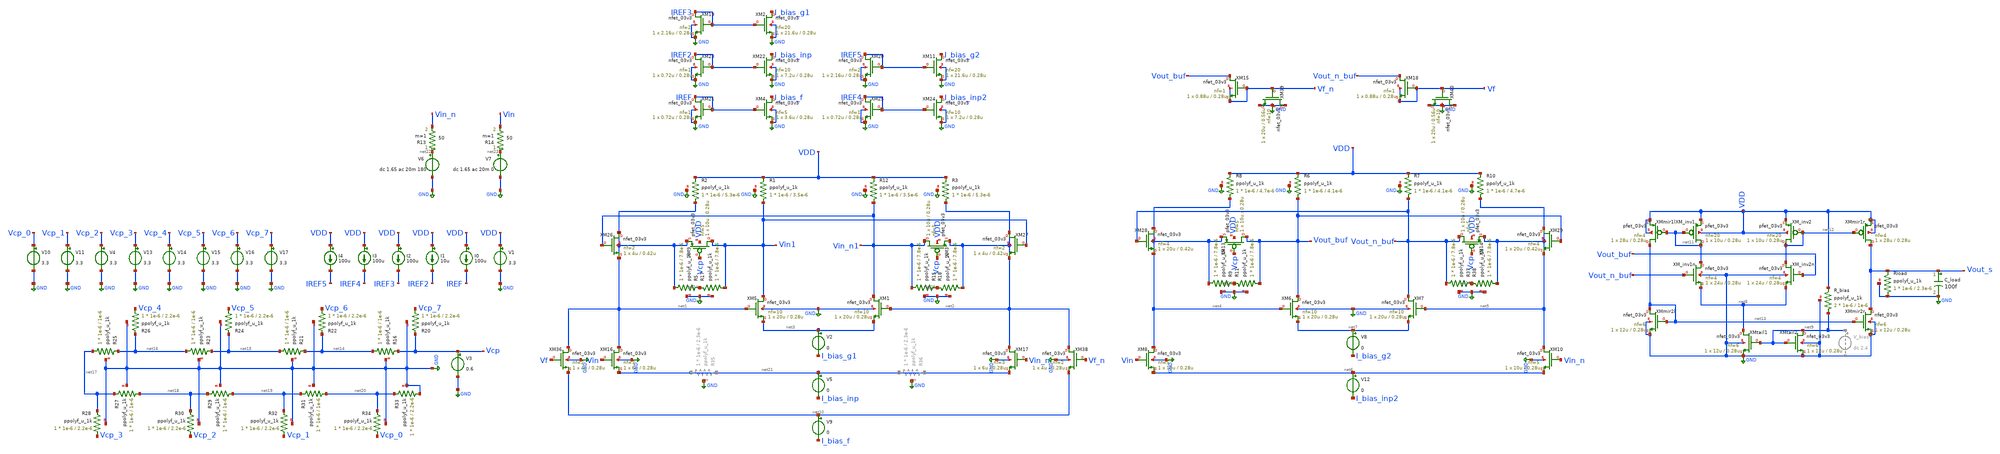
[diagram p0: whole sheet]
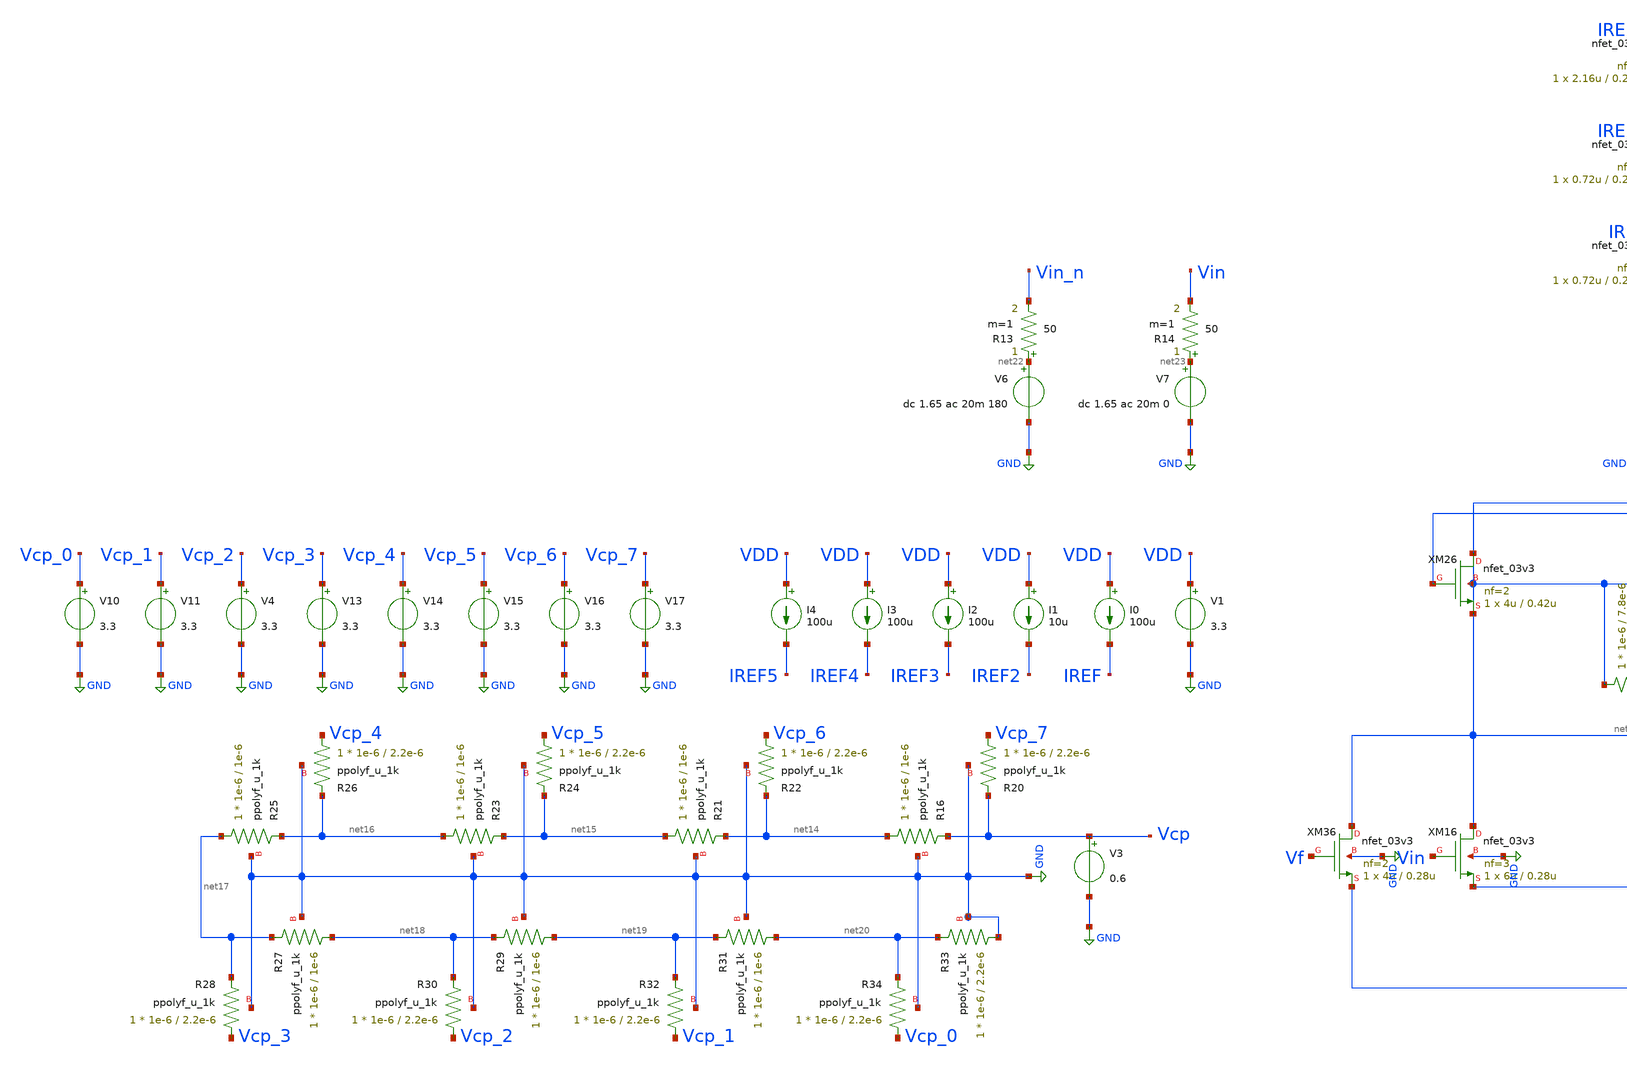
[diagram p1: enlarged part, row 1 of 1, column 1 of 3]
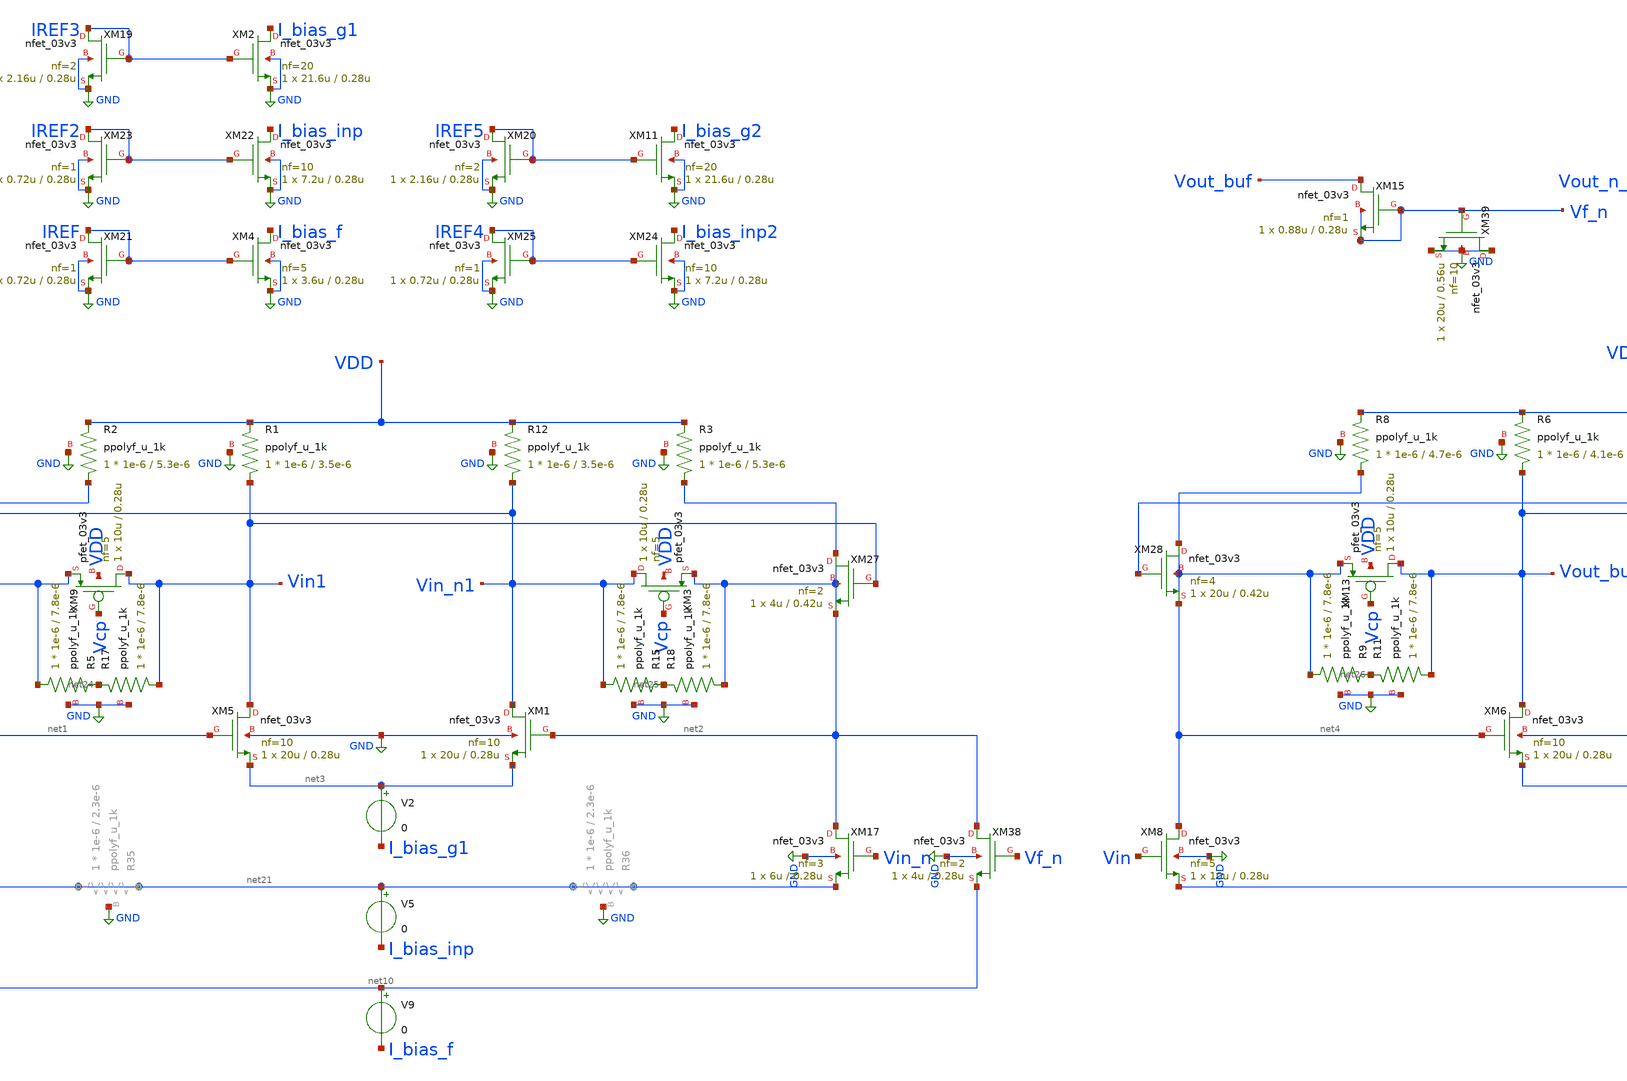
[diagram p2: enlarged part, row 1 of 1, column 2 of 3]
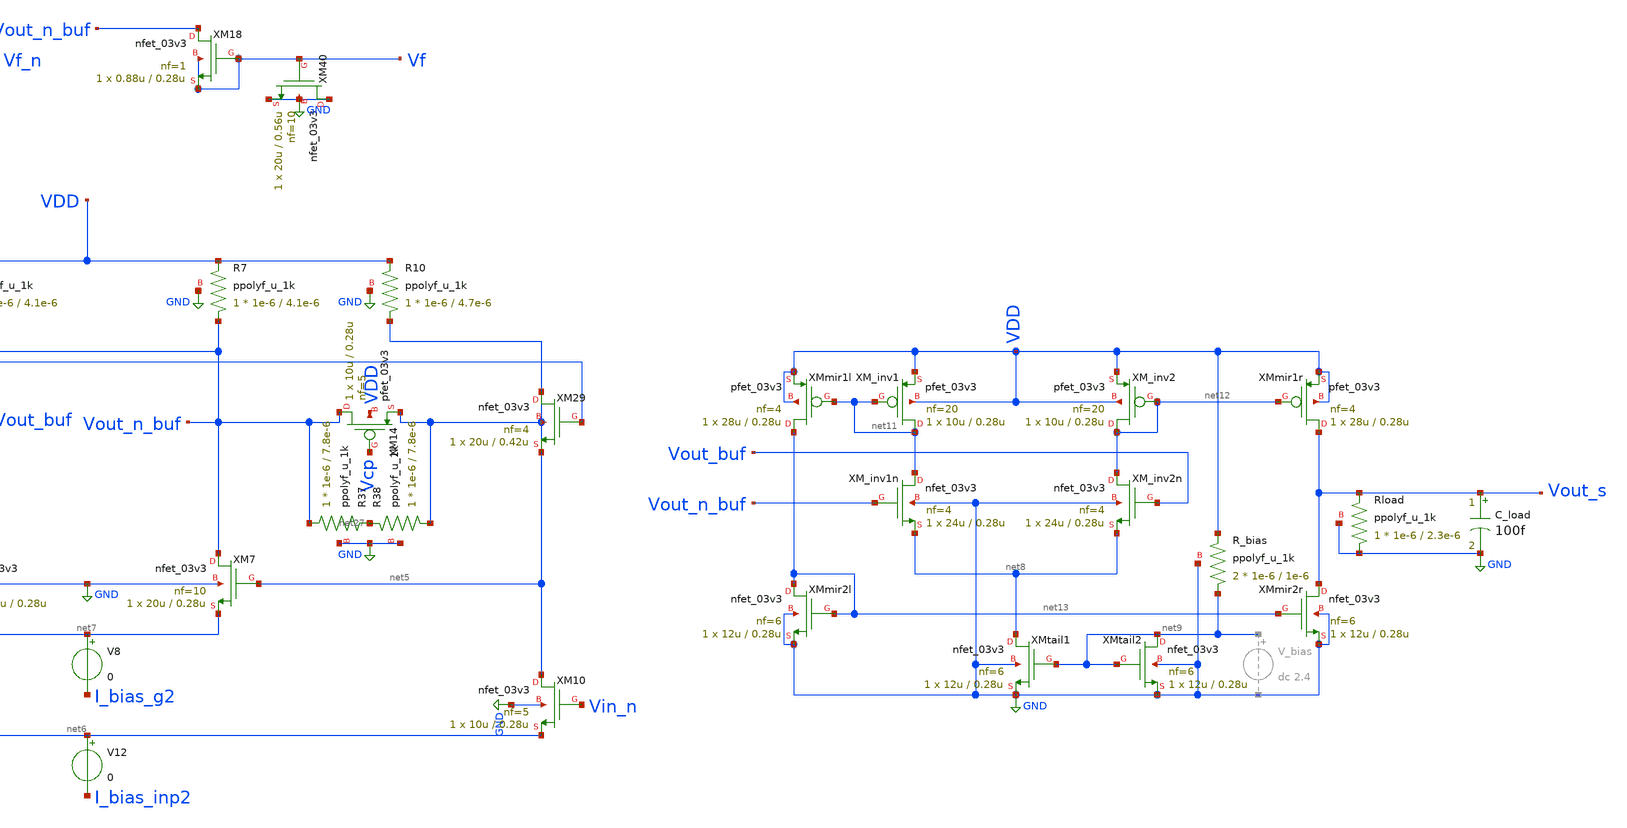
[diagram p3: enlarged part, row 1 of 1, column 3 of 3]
** sch_path: blocks/vga/vga.sch
**.subckt vga
V1 VDD GND 3.3
V6 net22 GND dc 1.65 ac 20m 180
XM5 Vin1 net1 net3 GND nfet_03v3 L=0.28u W=20u nf=10 ad='int((nf+1)/2) * W/nf * 0.18u' as='int((nf+2)/2) * W/nf * 0.18u'
+ pd='2*int((nf+1)/2) * (W/nf + 0.18u)' ps='2*int((nf+2)/2) * (W/nf + 0.18u)' nrd='0.18u / W' nrs='0.18u / W'
+ sa=0 sb=0 sd=0 m=1
XM1 Vin_n1 net2 net3 GND nfet_03v3 L=0.28u W=20u nf=10 ad='int((nf+1)/2) * W/nf * 0.18u' as='int((nf+2)/2) * W/nf * 0.18u'
+ pd='2*int((nf+1)/2) * (W/nf + 0.18u)' ps='2*int((nf+2)/2) * (W/nf + 0.18u)' nrd='0.18u / W' nrs='0.18u / W'
+ sa=0 sb=0 sd=0 m=1
XM16 net1 Vin net21 GND nfet_03v3 L=0.28u W=6u nf=3 ad='int((nf+1)/2) * W/nf * 0.18u' as='int((nf+2)/2) * W/nf * 0.18u'
+ pd='2*int((nf+1)/2) * (W/nf + 0.18u)' ps='2*int((nf+2)/2) * (W/nf + 0.18u)' nrd='0.18u / W' nrs='0.18u / W'
+ sa=0 sb=0 sd=0 m=1
XM17 net2 Vin_n net21 GND nfet_03v3 L=0.28u W=6u nf=3 ad='int((nf+1)/2) * W/nf * 0.18u' as='int((nf+2)/2) * W/nf * 0.18u'
+ pd='2*int((nf+1)/2) * (W/nf + 0.18u)' ps='2*int((nf+2)/2) * (W/nf + 0.18u)' nrd='0.18u / W' nrs='0.18u / W'
+ sa=0 sb=0 sd=0 m=1
XM9 Vin1 Vcp net1 VDD pfet_03v3 L=0.28u W=10u nf=5 ad='int((nf+1)/2) * W/nf * 0.18u' as='int((nf+2)/2) * W/nf * 0.18u'
+ pd='2*int((nf+1)/2) * (W/nf + 0.18u)' ps='2*int((nf+2)/2) * (W/nf + 0.18u)' nrd='0.18u / W' nrs='0.18u / W'
+ sa=0 sb=0 sd=0 m=1
XM6 Vout_buf net4 net7 GND nfet_03v3 L=0.28u W=20u nf=10 ad='int((nf+1)/2) * W/nf * 0.18u' as='int((nf+2)/2) * W/nf * 0.18u'
+ pd='2*int((nf+1)/2) * (W/nf + 0.18u)' ps='2*int((nf+2)/2) * (W/nf + 0.18u)' nrd='0.18u / W' nrs='0.18u / W'
+ sa=0 sb=0 sd=0 m=1
XM7 Vout_n_buf net5 net7 GND nfet_03v3 L=0.28u W=20u nf=10 ad='int((nf+1)/2) * W/nf * 0.18u' as='int((nf+2)/2) * W/nf * 0.18u'
+ pd='2*int((nf+1)/2) * (W/nf + 0.18u)' ps='2*int((nf+2)/2) * (W/nf + 0.18u)' nrd='0.18u / W' nrs='0.18u / W'
+ sa=0 sb=0 sd=0 m=1
XM8 net4 Vin net6 GND nfet_03v3 L=0.28u W=10u nf=5 ad='int((nf+1)/2) * W/nf * 0.18u' as='int((nf+2)/2) * W/nf * 0.18u'
+ pd='2*int((nf+1)/2) * (W/nf + 0.18u)' ps='2*int((nf+2)/2) * (W/nf + 0.18u)' nrd='0.18u / W' nrs='0.18u / W'
+ sa=0 sb=0 sd=0 m=1
XM10 net5 Vin_n net6 GND nfet_03v3 L=0.28u W=10u nf=5 ad='int((nf+1)/2) * W/nf * 0.18u' as='int((nf+2)/2) * W/nf * 0.18u'
+ pd='2*int((nf+1)/2) * (W/nf + 0.18u)' ps='2*int((nf+2)/2) * (W/nf + 0.18u)' nrd='0.18u / W' nrs='0.18u / W'
+ sa=0 sb=0 sd=0 m=1
V7 net23 GND dc 1.65 ac 20m 0
R14 net23 Vin 50 m=1
R13 net22 Vin_n 50 m=1
XM26 net1 Vin_n1 net1 net1 nfet_03v3 L=0.42u W=4u nf=2 ad='int((nf+1)/2) * W/nf * 0.18u' as='int((nf+2)/2) * W/nf * 0.18u'
+ pd='2*int((nf+1)/2) * (W/nf + 0.18u)' ps='2*int((nf+2)/2) * (W/nf + 0.18u)' nrd='0.18u / W' nrs='0.18u / W'
+ sa=0 sb=0 sd=0 m=1
XM27 net2 Vin1 net2 net2 nfet_03v3 L=0.42u W=4u nf=2 ad='int((nf+1)/2) * W/nf * 0.18u' as='int((nf+2)/2) * W/nf * 0.18u'
+ pd='2*int((nf+1)/2) * (W/nf + 0.18u)' ps='2*int((nf+2)/2) * (W/nf + 0.18u)' nrd='0.18u / W' nrs='0.18u / W'
+ sa=0 sb=0 sd=0 m=1
XM28 net4 Vout_n_buf net4 net4 nfet_03v3 L=0.42u W=20u nf=4 ad='int((nf+1)/2) * W/nf * 0.18u' as='int((nf+2)/2) * W/nf * 0.18u'
+ pd='2*int((nf+1)/2) * (W/nf + 0.18u)' ps='2*int((nf+2)/2) * (W/nf + 0.18u)' nrd='0.18u / W' nrs='0.18u / W'
+ sa=0 sb=0 sd=0 m=1
XM29 net5 Vout_buf net5 net5 nfet_03v3 L=0.42u W=20u nf=4 ad='int((nf+1)/2) * W/nf * 0.18u' as='int((nf+2)/2) * W/nf * 0.18u'
+ pd='2*int((nf+1)/2) * (W/nf + 0.18u)' ps='2*int((nf+2)/2) * (W/nf + 0.18u)' nrd='0.18u / W' nrs='0.18u / W'
+ sa=0 sb=0 sd=0 m=1
XM_inv1 net11 net11 VDD VDD pfet_03v3 L=0.28u W=10u nf=20 ad='int((nf+1)/2) * W/nf * 0.18u' as='int((nf+2)/2) * W/nf * 0.18u'
+ pd='2*int((nf+1)/2) * (W/nf + 0.18u)' ps='2*int((nf+2)/2) * (W/nf + 0.18u)' nrd='0.18u / W' nrs='0.18u / W'
+ sa=0 sb=0 sd=0 m=1
XM_inv1n net11 Vout_n_buf net8 GND nfet_03v3 L=0.28u W=24u nf=4 ad='int((nf+1)/2) * W/nf * 0.18u' as='int((nf+2)/2) * W/nf * 0.18u'
+ pd='2*int((nf+1)/2) * (W/nf + 0.18u)' ps='2*int((nf+2)/2) * (W/nf + 0.18u)' nrd='0.18u / W' nrs='0.18u / W'
+ sa=0 sb=0 sd=0 m=1
XM_inv2 net12 net12 VDD VDD pfet_03v3 L=0.28u W=10u nf=20 ad='int((nf+1)/2) * W/nf * 0.18u' as='int((nf+2)/2) * W/nf * 0.18u'
+ pd='2*int((nf+1)/2) * (W/nf + 0.18u)' ps='2*int((nf+2)/2) * (W/nf + 0.18u)' nrd='0.18u / W' nrs='0.18u / W'
+ sa=0 sb=0 sd=0 m=1
XM_inv2n net12 Vout_buf net8 GND nfet_03v3 L=0.28u W=24u nf=4 ad='int((nf+1)/2) * W/nf * 0.18u' as='int((nf+2)/2) * W/nf * 0.18u'
+ pd='2*int((nf+1)/2) * (W/nf + 0.18u)' ps='2*int((nf+2)/2) * (W/nf + 0.18u)' nrd='0.18u / W' nrs='0.18u / W'
+ sa=0 sb=0 sd=0 m=1
XMtail1 net8 net9 GND GND nfet_03v3 L=0.28u W=12u nf=6 ad='int((nf+1)/2) * W/nf * 0.18u' as='int((nf+2)/2) * W/nf * 0.18u'
+ pd='2*int((nf+1)/2) * (W/nf + 0.18u)' ps='2*int((nf+2)/2) * (W/nf + 0.18u)' nrd='0.18u / W' nrs='0.18u / W'
+ sa=0 sb=0 sd=0 m=1
XMtail2 net9 net9 GND GND nfet_03v3 L=0.28u W=12u nf=6 ad='int((nf+1)/2) * W/nf * 0.18u' as='int((nf+2)/2) * W/nf * 0.18u'
+ pd='2*int((nf+1)/2) * (W/nf + 0.18u)' ps='2*int((nf+2)/2) * (W/nf + 0.18u)' nrd='0.18u / W' nrs='0.18u / W'
+ sa=0 sb=0 sd=0 m=1
XM36 net1 Vf net10 GND nfet_03v3 L=0.28u W=4u nf=2 ad='int((nf+1)/2) * W/nf * 0.18u' as='int((nf+2)/2) * W/nf * 0.18u'
+ pd='2*int((nf+1)/2) * (W/nf + 0.18u)' ps='2*int((nf+2)/2) * (W/nf + 0.18u)' nrd='0.18u / W' nrs='0.18u / W'
+ sa=0 sb=0 sd=0 m=1
XM38 net2 Vf_n net10 GND nfet_03v3 L=0.28u W=4u nf=2 ad='int((nf+1)/2) * W/nf * 0.18u' as='int((nf+2)/2) * W/nf * 0.18u'
+ pd='2*int((nf+1)/2) * (W/nf + 0.18u)' ps='2*int((nf+2)/2) * (W/nf + 0.18u)' nrd='0.18u / W' nrs='0.18u / W'
+ sa=0 sb=0 sd=0 m=1
XM39 GND Vf_n GND GND nfet_03v3 L=0.56u W=20u nf=10 ad='int((nf+1)/2) * W/nf * 0.18u' as='int((nf+2)/2) * W/nf * 0.18u'
+ pd='2*int((nf+1)/2) * (W/nf + 0.18u)' ps='2*int((nf+2)/2) * (W/nf + 0.18u)' nrd='0.18u / W' nrs='0.18u / W'
+ sa=0 sb=0 sd=0 m=1
XM40 GND Vf GND GND nfet_03v3 L=0.56u W=20u nf=10 ad='int((nf+1)/2) * W/nf * 0.18u' as='int((nf+2)/2) * W/nf * 0.18u'
+ pd='2*int((nf+1)/2) * (W/nf + 0.18u)' ps='2*int((nf+2)/2) * (W/nf + 0.18u)' nrd='0.18u / W' nrs='0.18u / W'
+ sa=0 sb=0 sd=0 m=1
XMmir1l net13 net11 VDD VDD pfet_03v3 L=0.28u W=28u nf=4 ad='int((nf+1)/2) * W/nf * 0.18u' as='int((nf+2)/2) * W/nf * 0.18u'
+ pd='2*int((nf+1)/2) * (W/nf + 0.18u)' ps='2*int((nf+2)/2) * (W/nf + 0.18u)' nrd='0.18u / W' nrs='0.18u / W'
+ sa=0 sb=0 sd=0 m=1
XMmir1r Vout_s net12 VDD VDD pfet_03v3 L=0.28u W=28u nf=4 ad='int((nf+1)/2) * W/nf * 0.18u' as='int((nf+2)/2) * W/nf * 0.18u'
+ pd='2*int((nf+1)/2) * (W/nf + 0.18u)' ps='2*int((nf+2)/2) * (W/nf + 0.18u)' nrd='0.18u / W' nrs='0.18u / W'
+ sa=0 sb=0 sd=0 m=1
XMmir2l net13 net13 GND GND nfet_03v3 L=0.28u W=12u nf=6 ad='int((nf+1)/2) * W/nf * 0.18u' as='int((nf+2)/2) * W/nf * 0.18u'
+ pd='2*int((nf+1)/2) * (W/nf + 0.18u)' ps='2*int((nf+2)/2) * (W/nf + 0.18u)' nrd='0.18u / W' nrs='0.18u / W'
+ sa=0 sb=0 sd=0 m=1
XMmir2r Vout_s net13 GND GND nfet_03v3 L=0.28u W=12u nf=6 ad='int((nf+1)/2) * W/nf * 0.18u' as='int((nf+2)/2) * W/nf * 0.18u'
+ pd='2*int((nf+1)/2) * (W/nf + 0.18u)' ps='2*int((nf+2)/2) * (W/nf + 0.18u)' nrd='0.18u / W' nrs='0.18u / W'
+ sa=0 sb=0 sd=0 m=1
XR_bias net9 VDD GND ppolyf_u_1k r_width=1e-6 r_length=1e-6 m=2
C_load Vout_s GND 100f m=1
XR16 net14 Vcp GND ppolyf_u_1k r_width=1e-6 r_length=1e-6 m=1
XR20 Vcp_7 Vcp GND ppolyf_u_1k r_width=1e-6 r_length=2.2e-6 m=1
XR21 net15 net14 GND ppolyf_u_1k r_width=1e-6 r_length=1e-6 m=1
XR22 Vcp_6 net14 GND ppolyf_u_1k r_width=1e-6 r_length=2.2e-6 m=1
XR23 net16 net15 GND ppolyf_u_1k r_width=1e-6 r_length=1e-6 m=1
XR24 Vcp_5 net15 GND ppolyf_u_1k r_width=1e-6 r_length=2.2e-6 m=1
XR25 net17 net16 GND ppolyf_u_1k r_width=1e-6 r_length=1e-6 m=1
XR26 Vcp_4 net16 GND ppolyf_u_1k r_width=1e-6 r_length=2.2e-6 m=1
XR27 net18 net17 GND ppolyf_u_1k r_width=1e-6 r_length=1e-6 m=1
XR28 Vcp_3 net17 GND ppolyf_u_1k r_width=1e-6 r_length=2.2e-6 m=1
XR29 net19 net18 GND ppolyf_u_1k r_width=1e-6 r_length=1e-6 m=1
XR30 Vcp_2 net18 GND ppolyf_u_1k r_width=1e-6 r_length=2.2e-6 m=1
XR31 net20 net19 GND ppolyf_u_1k r_width=1e-6 r_length=1e-6 m=1
XR32 Vcp_1 net19 GND ppolyf_u_1k r_width=1e-6 r_length=2.2e-6 m=1
XR33 GND net20 GND ppolyf_u_1k r_width=1e-6 r_length=2.2e-6 m=1
XR34 Vcp_0 net20 GND ppolyf_u_1k r_width=1e-6 r_length=2.2e-6 m=1
V10 Vcp_0 GND 3.3
V11 Vcp_1 GND 3.3
V4 Vcp_2 GND 3.3
V13 Vcp_3 GND 3.3
V14 Vcp_4 GND 3.3
V15 Vcp_5 GND 3.3
V16 Vcp_6 GND 3.3
V17 Vcp_7 GND 3.3
V3 Vcp GND 0.6
XM15 Vout_buf Vf_n Vf_n Vf_n nfet_03v3 L=0.28u W=0.88u nf=1 ad='int((nf+1)/2) * W/nf * 0.18u' as='int((nf+2)/2) * W/nf * 0.18u'
+ pd='2*int((nf+1)/2) * (W/nf + 0.18u)' ps='2*int((nf+2)/2) * (W/nf + 0.18u)' nrd='0.18u / W' nrs='0.18u / W'
+ sa=0 sb=0 sd=0 m=1
XM18 Vout_n_buf Vf Vf Vf nfet_03v3 L=0.28u W=0.88u nf=1 ad='int((nf+1)/2) * W/nf * 0.18u' as='int((nf+2)/2) * W/nf * 0.18u'
+ pd='2*int((nf+1)/2) * (W/nf + 0.18u)' ps='2*int((nf+2)/2) * (W/nf + 0.18u)' nrd='0.18u / W' nrs='0.18u / W'
+ sa=0 sb=0 sd=0 m=1
XR5 net1 net24 GND ppolyf_u_1k r_width=1e-6 r_length=7.8e-6 m=1
XR17 Vin1 net24 GND ppolyf_u_1k r_width=1e-6 r_length=7.8e-6 m=1
XM3 Vin_n1 Vcp net2 VDD pfet_03v3 L=0.28u W=10u nf=5 ad='int((nf+1)/2) * W/nf * 0.18u' as='int((nf+2)/2) * W/nf * 0.18u'
+ pd='2*int((nf+1)/2) * (W/nf + 0.18u)' ps='2*int((nf+2)/2) * (W/nf + 0.18u)' nrd='0.18u / W' nrs='0.18u / W'
+ sa=0 sb=0 sd=0 m=1
XR15 Vin_n1 net25 GND ppolyf_u_1k r_width=1e-6 r_length=7.8e-6 m=1
XR18 net2 net25 GND ppolyf_u_1k r_width=1e-6 r_length=7.8e-6 m=1
XM13 Vout_buf Vcp net4 VDD pfet_03v3 L=0.28u W=10u nf=5 ad='int((nf+1)/2) * W/nf * 0.18u' as='int((nf+2)/2) * W/nf * 0.18u'
+ pd='2*int((nf+1)/2) * (W/nf + 0.18u)' ps='2*int((nf+2)/2) * (W/nf + 0.18u)' nrd='0.18u / W' nrs='0.18u / W'
+ sa=0 sb=0 sd=0 m=1
XR9 net4 net26 GND ppolyf_u_1k r_width=1e-6 r_length=7.8e-6 m=1
XR11 Vout_buf net26 GND ppolyf_u_1k r_width=1e-6 r_length=7.8e-6 m=1
XM14 Vout_n_buf Vcp net5 VDD pfet_03v3 L=0.28u W=10u nf=5 ad='int((nf+1)/2) * W/nf * 0.18u' as='int((nf+2)/2) * W/nf * 0.18u'
+ pd='2*int((nf+1)/2) * (W/nf + 0.18u)' ps='2*int((nf+2)/2) * (W/nf + 0.18u)' nrd='0.18u / W' nrs='0.18u / W'
+ sa=0 sb=0 sd=0 m=1
XR37 Vout_n_buf net27 GND ppolyf_u_1k r_width=1e-6 r_length=7.8e-6 m=1
XR38 net5 net27 GND ppolyf_u_1k r_width=1e-6 r_length=7.8e-6 m=1
XRload GND Vout_s GND ppolyf_u_1k r_width=1e-6 r_length=2.3e-6 m=1
XR1 Vin1 VDD GND ppolyf_u_1k r_width=1e-6 r_length=3.5e-6 m=1
XR12 Vin_n1 VDD GND ppolyf_u_1k r_width=1e-6 r_length=3.5e-6 m=1
XR6 Vout_buf VDD GND ppolyf_u_1k r_width=1e-6 r_length=4.1e-6 m=1
XR7 Vout_n_buf VDD GND ppolyf_u_1k r_width=1e-6 r_length=4.1e-6 m=1
XR3 net2 VDD GND ppolyf_u_1k r_width=1e-6 r_length=5.3e-6 m=1
XR2 net1 VDD GND ppolyf_u_1k r_width=1e-6 r_length=5.3e-6 m=1
XR8 net4 VDD GND ppolyf_u_1k r_width=1e-6 r_length=4.7e-6 m=1
XR10 net5 VDD GND ppolyf_u_1k r_width=1e-6 r_length=4.7e-6 m=1
I0 VDD IREF 100u
XM2 I_bias_g1 IREF3 GND GND nfet_03v3 L=0.28u W=21.6u nf=20 ad='int((nf+1)/2) * W/nf * 0.18u' as='int((nf+2)/2) * W/nf * 0.18u'
+ pd='2*int((nf+1)/2) * (W/nf + 0.18u)' ps='2*int((nf+2)/2) * (W/nf + 0.18u)' nrd='0.18u / W' nrs='0.18u / W'
+ sa=0 sb=0 sd=0 m=1
XM19 IREF3 IREF3 GND GND nfet_03v3 L=0.28u W=2.16u nf=2 ad='int((nf+1)/2) * W/nf * 0.18u' as='int((nf+2)/2) * W/nf * 0.18u'
+ pd='2*int((nf+1)/2) * (W/nf + 0.18u)' ps='2*int((nf+2)/2) * (W/nf + 0.18u)' nrd='0.18u / W' nrs='0.18u / W'
+ sa=0 sb=0 sd=0 m=1
XM11 I_bias_g2 IREF5 GND GND nfet_03v3 L=0.28u W=21.6u nf=20 ad='int((nf+1)/2) * W/nf * 0.18u' as='int((nf+2)/2) * W/nf * 0.18u'
+ pd='2*int((nf+1)/2) * (W/nf + 0.18u)' ps='2*int((nf+2)/2) * (W/nf + 0.18u)' nrd='0.18u / W' nrs='0.18u / W'
+ sa=0 sb=0 sd=0 m=1
XM20 IREF5 IREF5 GND GND nfet_03v3 L=0.28u W=2.16u nf=2 ad='int((nf+1)/2) * W/nf * 0.18u' as='int((nf+2)/2) * W/nf * 0.18u'
+ pd='2*int((nf+1)/2) * (W/nf + 0.18u)' ps='2*int((nf+2)/2) * (W/nf + 0.18u)' nrd='0.18u / W' nrs='0.18u / W'
+ sa=0 sb=0 sd=0 m=1
V2 net3 I_bias_g1 0
XM22 I_bias_inp IREF2 GND GND nfet_03v3 L=0.28u W=7.2u nf=10 ad='int((nf+1)/2) * W/nf * 0.18u' as='int((nf+2)/2) * W/nf * 0.18u'
+ pd='2*int((nf+1)/2) * (W/nf + 0.18u)' ps='2*int((nf+2)/2) * (W/nf + 0.18u)' nrd='0.18u / W' nrs='0.18u / W'
+ sa=0 sb=0 sd=0 m=1
XM23 IREF2 IREF2 GND GND nfet_03v3 L=0.28u W=0.72u nf=1 ad='int((nf+1)/2) * W/nf * 0.18u' as='int((nf+2)/2) * W/nf * 0.18u'
+ pd='2*int((nf+1)/2) * (W/nf + 0.18u)' ps='2*int((nf+2)/2) * (W/nf + 0.18u)' nrd='0.18u / W' nrs='0.18u / W'
+ sa=0 sb=0 sd=0 m=1
V5 net21 I_bias_inp 0
I1 VDD IREF2 10u
I2 VDD IREF3 100u
V8 net7 I_bias_g2 0
XM4 I_bias_f IREF GND GND nfet_03v3 L=0.28u W=3.6u nf=5 ad='int((nf+1)/2) * W/nf * 0.18u' as='int((nf+2)/2) * W/nf * 0.18u'
+ pd='2*int((nf+1)/2) * (W/nf + 0.18u)' ps='2*int((nf+2)/2) * (W/nf + 0.18u)' nrd='0.18u / W' nrs='0.18u / W'
+ sa=0 sb=0 sd=0 m=1
XM21 IREF IREF GND GND nfet_03v3 L=0.28u W=0.72u nf=1 ad='int((nf+1)/2) * W/nf * 0.18u' as='int((nf+2)/2) * W/nf * 0.18u'
+ pd='2*int((nf+1)/2) * (W/nf + 0.18u)' ps='2*int((nf+2)/2) * (W/nf + 0.18u)' nrd='0.18u / W' nrs='0.18u / W'
+ sa=0 sb=0 sd=0 m=1
I3 VDD IREF4 100u
V9 net10 I_bias_f 0
XM24 I_bias_inp2 IREF4 GND GND nfet_03v3 L=0.28u W=7.2u nf=10 ad='int((nf+1)/2) * W/nf * 0.18u' as='int((nf+2)/2) * W/nf * 0.18u'
+ pd='2*int((nf+1)/2) * (W/nf + 0.18u)' ps='2*int((nf+2)/2) * (W/nf + 0.18u)' nrd='0.18u / W' nrs='0.18u / W'
+ sa=0 sb=0 sd=0 m=1
XM25 IREF4 IREF4 GND GND nfet_03v3 L=0.28u W=0.72u nf=1 ad='int((nf+1)/2) * W/nf * 0.18u' as='int((nf+2)/2) * W/nf * 0.18u'
+ pd='2*int((nf+1)/2) * (W/nf + 0.18u)' ps='2*int((nf+2)/2) * (W/nf + 0.18u)' nrd='0.18u / W' nrs='0.18u / W'
+ sa=0 sb=0 sd=0 m=1
I4 VDD IREF5 100u
V12 net6 I_bias_inp2 0
**** begin user architecture code


.include /foss/pdks/gf180mcuD/libs.tech/ngspice/design.ngspice
.lib /foss/pdks/gf180mcuD/libs.tech/ngspice/sm141064.ngspice typical
.lib /foss/pdks/gf180mcuD/libs.tech/ngspice/sm141064.ngspice bjt_typical
.lib /foss/pdks/gf180mcuD/libs.tech/ngspice/sm141064.ngspice diode_typical
.lib /foss/pdks/gf180mcuD/libs.tech/ngspice/sm141064.ngspice res_typical
.lib /foss/pdks/gf180mcuD/libs.tech/ngspice/sm141064.ngspice mimcap_typical
.lib /foss/pdks/gf180mcuD/libs.tech/ngspice/sm141064.ngspice moscap_typical
.option method=gear

.control
set temp = 25
  * 1. Setup the sweep parameters
  let v_ctrl = 0.6

  let f_start = 1
  let f_stop = 3.2G
  let f_points = 120

  * 2. Initialize vectors to store results
  let gain_db = unitvec(f_points)

  alter v3 = v_ctrl
  ac dec $&f_points $&f_start $&f_stop

  * 4. Calculate Differential Gain in dB
  * Formula: 20 * log10(|Vout_diff| / |Vin_diff|)
  let vin_mag = mag(v(vin) - v(vin_n))
  let vout_s_mag = mag(v(vout_s))
  let vout_buf_mag = mag(v(vout_buf) - v(vout_n_buf))
  let vout_s_gain = 20 * log10(vout_s_mag / vin_mag)
  let vout_buf_gain = 20 * log10(vout_buf_mag / vin_mag)

  * Credit to marcel hendrix
  * https://sourceforge.net/p/ngspice/discussion/133842/thread/2031ad61/
  meas ac peak  MAX  vmag(vout_s) FROM=$&f_start TO=$&f_stop
  let f3db = peak/sqrt(2)
  meas ac lo_3db WHEN vmag(vout_s)=f3db RISE=1
  meas ac hi_3db WHEN vmag(vout_s)=f3db FALL=1

  * 5. Save results to vectors
  plot vout_s_gain vout_buf_gain title 'Gain (dB) vs. Frequency from 1MHz to 3.2GHz, 0.6 vctrl' ylimit
+ 0 80
.endc


**** end user architecture code
**.ends
.GLOBAL GND
.end
